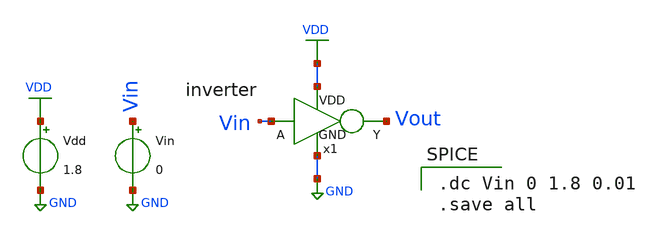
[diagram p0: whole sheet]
** sch_path: designs/inverter/xschem/inverter_tb.sch
**.subckt inverter_tb
Vdd VDD GND 1.8
Vin Vin GND 0
x1 VDD Vin Vout GND inverter
**** begin user architecture code

** opencircuidesign pdks install
.lib /home/ubvm/Desktop/chip_design/open_pdks/sky130/sky130A/libs.tech/ngspice/sky130.lib.spice tt_mm




.dc Vin 0 1.8 0.01
.save all

**** end user architecture code
**.ends

* expanding   symbol:  inverter.sym # of pins=4
** sym_path: designs/inverter/xschem/inverter.sym
** sch_path: designs/inverter/xschem/inverter.sch
.subckt inverter VDD A Y GND
input p1
output p2
inout p3
inout p4
XM1 net1 net2 net4 net4 sky130_fd_pr__nfet_01v8 L=0.15 W=1 nf=1 ad='int((1 + 1)/2) * 1 / 1 * 0.29' as='int((1 + 2)/2) * 1 / 1 * 0.29'
+ pd='2*int((1 + 1)/2) * (1 / 1 + 0.29)' ps='2*int((1 + 2)/2) * (1 / 1 + 0.29)' nrd='0.29 / 1 ' nrs='0.29 / 1 '
+ sa=0 sb=0 sd=0 mult=1 m=1
XM2 net1 net2 net3 net3 sky130_fd_pr__pfet_01v8 L=0.15 W=1 nf=1 ad='int((1 + 1)/2) * 1 / 1 * 0.29' as='int((1 + 2)/2) * 1 / 1 * 0.29'
+ pd='2*int((1 + 1)/2) * (1 / 1 + 0.29)' ps='2*int((1 + 2)/2) * (1 / 1 + 0.29)' nrd='0.29 / 1 ' nrs='0.29 / 1 '
+ sa=0 sb=0 sd=0 mult=1 m=1
.ends

.GLOBAL VDD
.GLOBAL GND
.end
